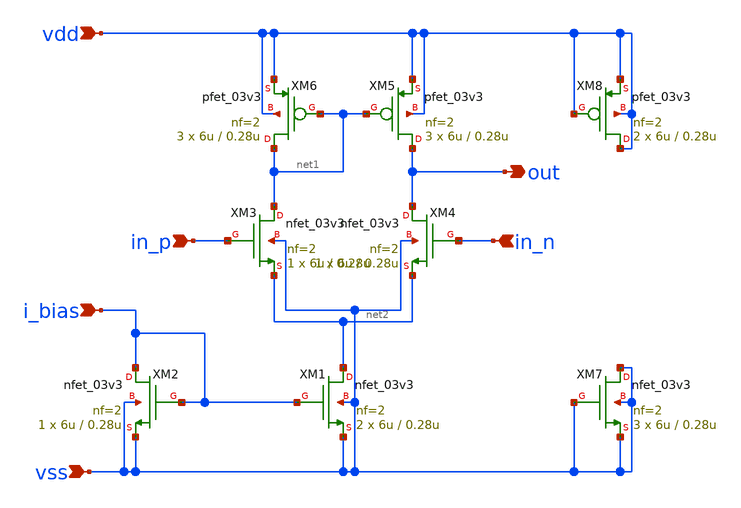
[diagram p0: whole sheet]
** sch_path: designs/libs/xp_core_analog/ota_5t/ota_5t.sch
**.subckt ota_5t in_p in_n i_bias vdd vss out
*.ipin in_p
*.ipin in_n
*.ipin i_bias
*.ipin vdd
*.ipin vss
*.opin out
XM1 net2 i_bias vss vss nfet_03v3 L=0.28u W=6u nf=2 ad='int((nf+1)/2) * W/nf * 0.18u' as='int((nf+2)/2) * W/nf * 0.18u'
+ pd='2*int((nf+1)/2) * (W/nf + 0.18u)' ps='2*int((nf+2)/2) * (W/nf + 0.18u)' nrd='0.18u / W' nrs='0.18u / W'
+ sa=0 sb=0 sd=0 m=2
XM2 i_bias i_bias vss vss nfet_03v3 L=0.28u W=6u nf=2 ad='int((nf+1)/2) * W/nf * 0.18u' as='int((nf+2)/2) * W/nf * 0.18u'
+ pd='2*int((nf+1)/2) * (W/nf + 0.18u)' ps='2*int((nf+2)/2) * (W/nf + 0.18u)' nrd='0.18u / W' nrs='0.18u / W'
+ sa=0 sb=0 sd=0 m=1
XM3 net1 in_p net2 vss nfet_03v3 L=0.28u W=6u nf=2 ad='int((nf+1)/2) * W/nf * 0.18u' as='int((nf+2)/2) * W/nf * 0.18u'
+ pd='2*int((nf+1)/2) * (W/nf + 0.18u)' ps='2*int((nf+2)/2) * (W/nf + 0.18u)' nrd='0.18u / W' nrs='0.18u / W'
+ sa=0 sb=0 sd=0 m=1
XM4 out in_n net2 vss nfet_03v3 L=0.28u W=6u nf=2 ad='int((nf+1)/2) * W/nf * 0.18u' as='int((nf+2)/2) * W/nf * 0.18u'
+ pd='2*int((nf+1)/2) * (W/nf + 0.18u)' ps='2*int((nf+2)/2) * (W/nf + 0.18u)' nrd='0.18u / W' nrs='0.18u / W'
+ sa=0 sb=0 sd=0 m=1
XM5 out net1 vdd vdd pfet_03v3 L=0.28u W=6u nf=2 ad='int((nf+1)/2) * W/nf * 0.18u' as='int((nf+2)/2) * W/nf * 0.18u'
+ pd='2*int((nf+1)/2) * (W/nf + 0.18u)' ps='2*int((nf+2)/2) * (W/nf + 0.18u)' nrd='0.18u / W' nrs='0.18u / W'
+ sa=0 sb=0 sd=0 m=3
XM6 net1 net1 vdd vdd pfet_03v3 L=0.28u W=6u nf=2 ad='int((nf+1)/2) * W/nf * 0.18u' as='int((nf+2)/2) * W/nf * 0.18u'
+ pd='2*int((nf+1)/2) * (W/nf + 0.18u)' ps='2*int((nf+2)/2) * (W/nf + 0.18u)' nrd='0.18u / W' nrs='0.18u / W'
+ sa=0 sb=0 sd=0 m=3
XM7 vss vss vss vss nfet_03v3 L=0.28u W=6u nf=2 ad='int((nf+1)/2) * W/nf * 0.18u' as='int((nf+2)/2) * W/nf * 0.18u'
+ pd='2*int((nf+1)/2) * (W/nf + 0.18u)' ps='2*int((nf+2)/2) * (W/nf + 0.18u)' nrd='0.18u / W' nrs='0.18u / W'
+ sa=0 sb=0 sd=0 m=3
XM8 vdd vdd vdd vdd pfet_03v3 L=0.28u W=6u nf=2 ad='int((nf+1)/2) * W/nf * 0.18u' as='int((nf+2)/2) * W/nf * 0.18u'
+ pd='2*int((nf+1)/2) * (W/nf + 0.18u)' ps='2*int((nf+2)/2) * (W/nf + 0.18u)' nrd='0.18u / W' nrs='0.18u / W'
+ sa=0 sb=0 sd=0 m=2
**.ends
.end
